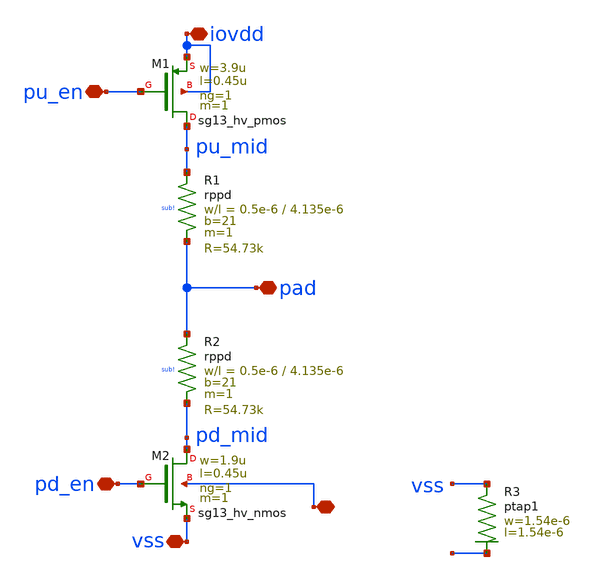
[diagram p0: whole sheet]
** sch_path: ihp-sg13g2/libs.tech/xschem/hm_stdcells/hm_PUPD_noptap.sch
**.subckt hm_PUPD_noptap pad pu_en pd_en iovdd ! vss
*.iopin pad
*.iopin pu_en
*.iopin pd_en
*.iopin iovdd
*.iopin !
*.iopin vss
XM1 pu_mid pu_en iovdd iovdd sg13_hv_pmos w=3.9u l=0.45u ng=1 m=1 mm_ok=1
XM2 pd_mid pd_en vss ! sg13_hv_nmos w=1.9u l=0.45u ng=1 m=1 mm_ok=1
XR1 pu_mid pad sub! rppd w=0.5e-6 l=4.135e-6 m=1 b=21 mm_ok=1
XR2 pad pd_mid sub! rppd w=0.5e-6 l=4.135e-6 m=1 b=21 mm_ok=1
XR3 vss ! ptap1 R=114.9 w=1.54e-6 l=1.54e-6
**.ends
.end
